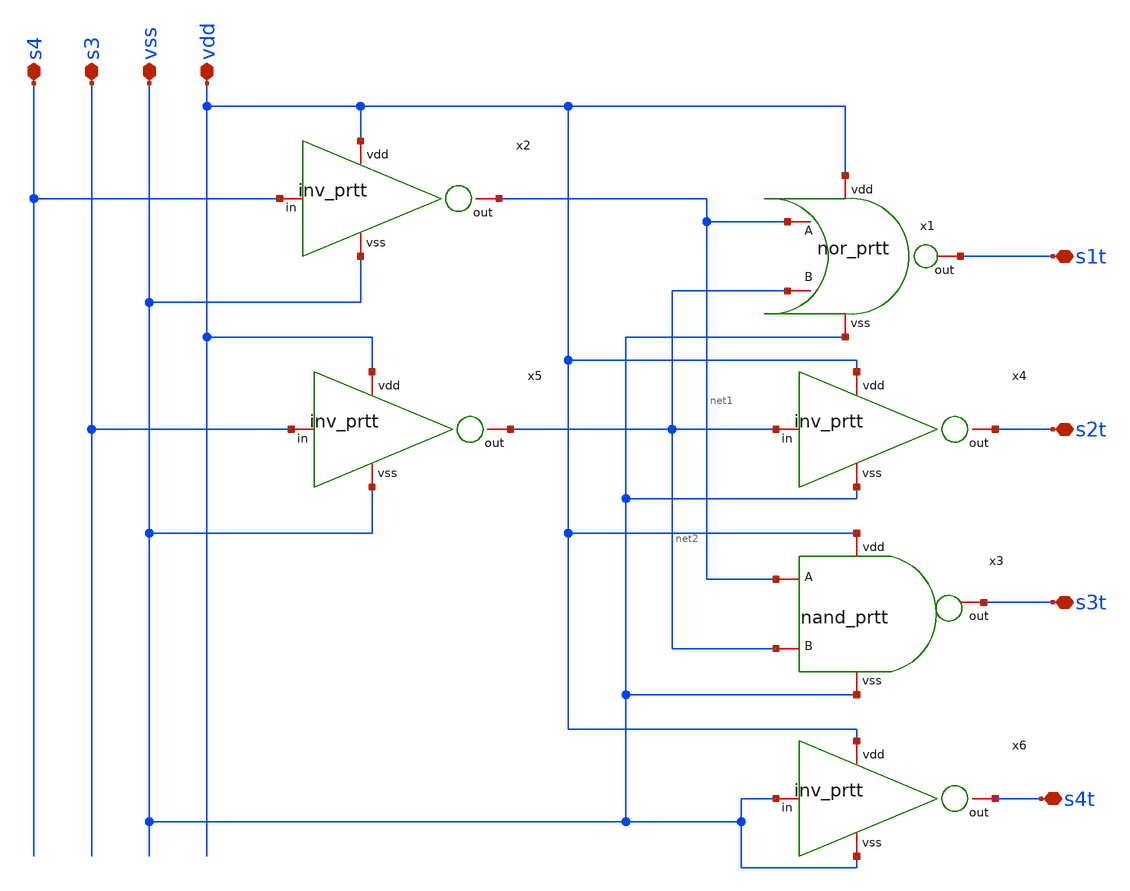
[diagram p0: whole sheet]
** sch_path: BinarytoThermo/Circuit_stdcells.sch
**.subckt Circuit_stdcells s4 s3 s1t s2t s3t s4t vdd vss
*.iopin s4
*.iopin s3
*.iopin s1t
*.iopin s2t
*.iopin s3t
*.iopin s4t
*.iopin vdd
*.iopin vss
x3 vdd s3t net1 net2 vss nand_prtt
x1 vdd net1 s1t net2 vss nor_prtt
x2 vdd s4 net1 vss inv_prtt
x4 vdd net2 s2t vss inv_prtt
x5 vdd s3 net2 vss inv_prtt
x6 vdd vss s4t vss inv_prtt
**.ends
.end
